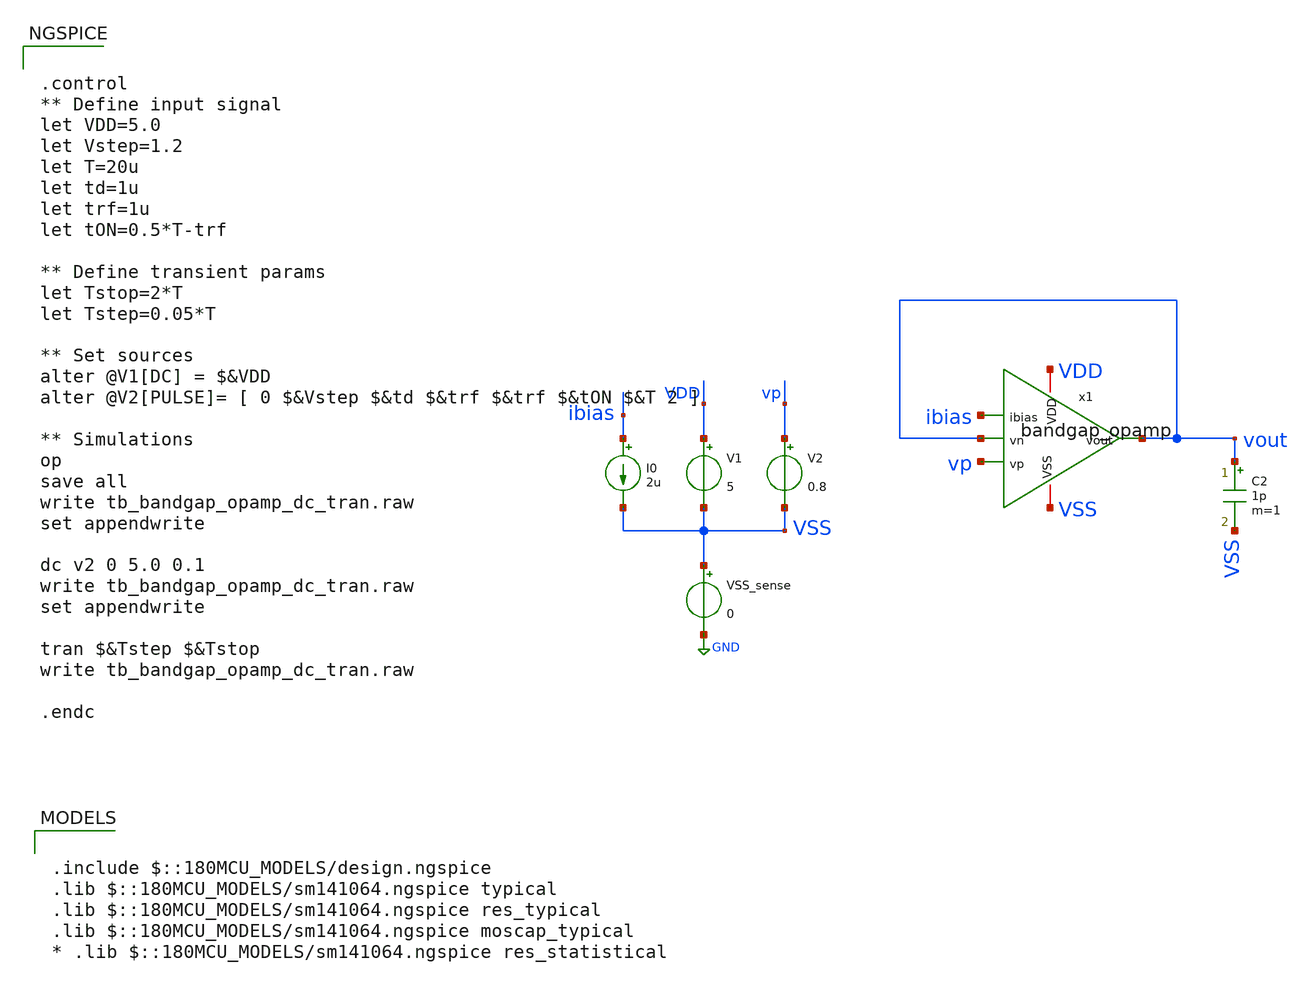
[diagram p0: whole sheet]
** sch_path: designs/libs/tb_bandgap/tb_bandgap_opamp_dc_tran/tb_bandgap_opamp_dc_tran.sch
**.subckt tb_bandgap_opamp_dc_tran
V1 VDD VSS 5
V2 vp VSS 0.8
VSS_sense VSS GND 0
C2 vout VSS 1p m=1
I0 ibias VSS 2u
x1 VDD ibias vout vp vout VSS bandgap_opamp
**** begin user architecture code

.include $::180MCU_MODELS/design.ngspice
.lib $::180MCU_MODELS/sm141064.ngspice typical
.lib $::180MCU_MODELS/sm141064.ngspice res_typical
.lib $::180MCU_MODELS/sm141064.ngspice moscap_typical
* .lib $::180MCU_MODELS/sm141064.ngspice res_statistical



.control
** Define input signal
let VDD=5.0
let Vstep=1.2
let T=20u
let td=1u
let trf=1u
let tON=0.5*T-trf

** Define transient params
let Tstop=2*T
let Tstep=0.05*T

** Set sources
alter @V1[DC] = $&VDD
alter @V2[PULSE]= [ 0 $&Vstep $&td $&trf $&trf $&tON $&T 2 ]

** Simulations
op
save all
write tb_bandgap_opamp_dc_tran.raw
set appendwrite

dc v2 0 5.0 0.1
write tb_bandgap_opamp_dc_tran.raw
set appendwrite

tran $&Tstep $&Tstop
write tb_bandgap_opamp_dc_tran.raw

.endc


**** end user architecture code
**.ends
.GLOBAL GND
.end
